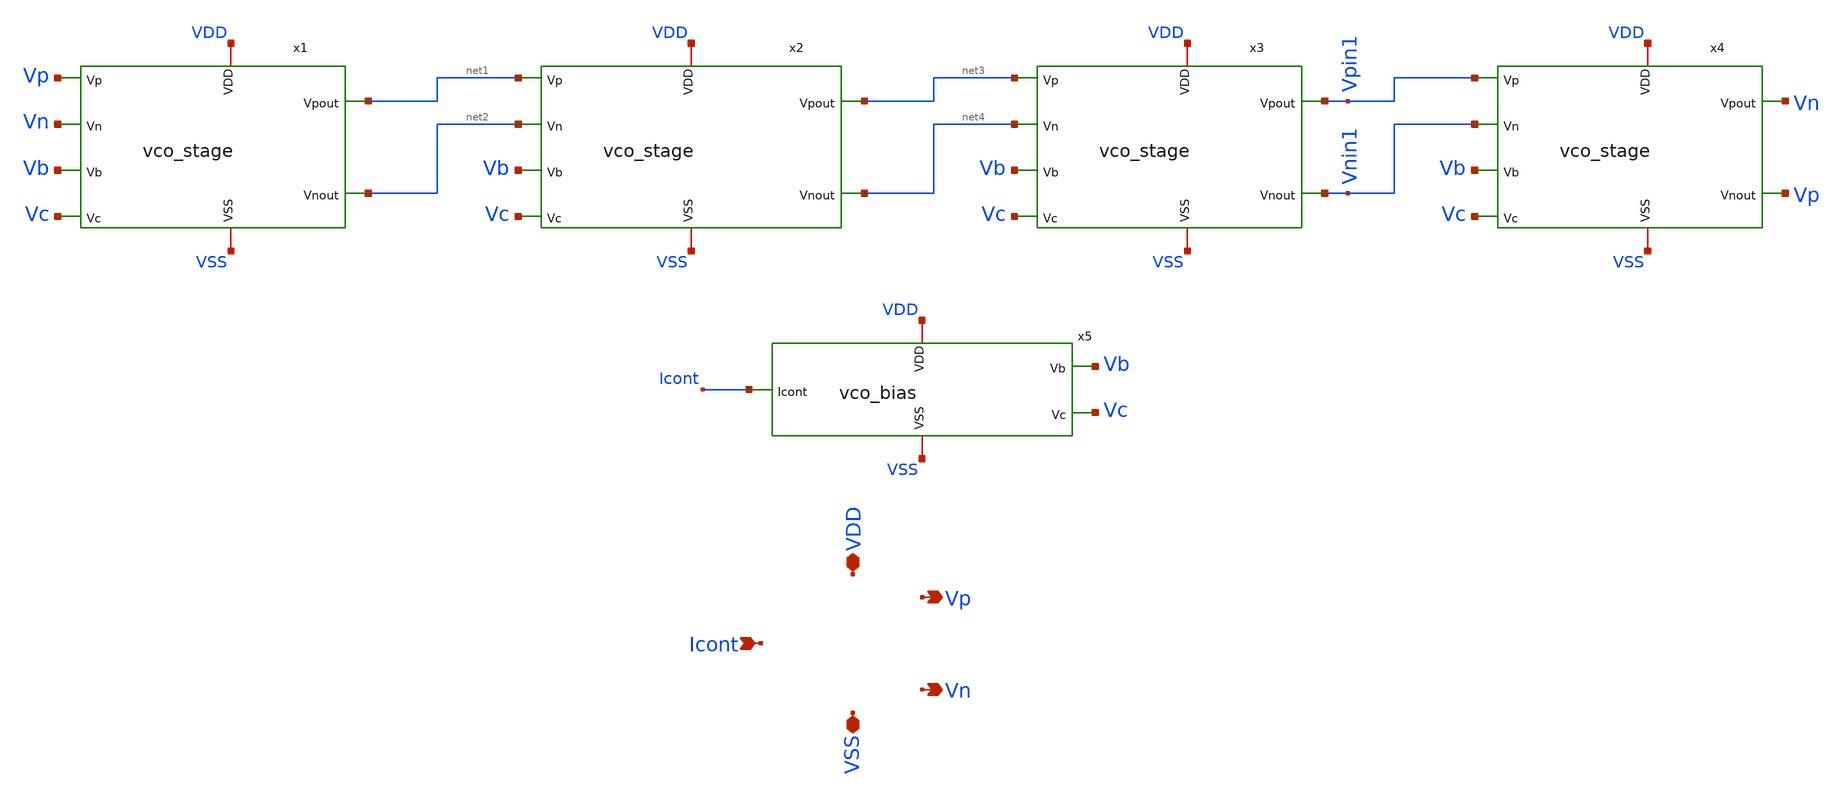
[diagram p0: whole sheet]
** sch_path: xschem/vco.sch
**.subckt vco VDD VSS Icont Vp Vn
*.iopin VDD
*.iopin VSS
*.ipin Icont
*.opin Vp
*.opin Vn
x1 VDD VSS Vp Vn Vb Vc net1 net2 vco_stage
x2 VDD VSS net1 net2 Vb Vc net3 net4 vco_stage
x3 VDD VSS net3 net4 Vb Vc Vpin1 Vnin1 vco_stage
x4 VDD VSS Vpin1 Vnin1 Vb Vc Vn Vp vco_stage
x5 VDD VSS Icont Vb Vc vco_bias
**.ends

* expanding   symbol:  vco_stage.sym # of pins=8
** sym_path: xschem/vco_stage.sym
** sch_path: xschem/vco_stage.sch
.subckt vco_stage VDD VSS Vp Vn Vb Vc Vpout Vnout
*.iopin VDD
*.iopin VSS
*.ipin Vp
*.ipin Vn
*.ipin Vb
*.ipin Vc
*.opin Vpout
*.opin Vnout
XM5 Vds_m5 Vc VSS VSS sky130_fd_pr__nfet_01v8 L={L} W={W} nf=2 ad='int((nf+1)/2) * W/nf * 0.29' as='int((nf+2)/2) * W/nf * 0.29'
+ pd='2*int((nf+1)/2) * (W/nf + 0.29)' ps='2*int((nf+2)/2) * (W/nf + 0.29)' nrd='0.29 / W' nrs='0.29 / W'
+ sa=0 sb=0 sd=0 mult=1 m=1
x1 VDD VSS Vp Vb Vnout Vpout Vds_m5 vco_stage_half
x2 VDD VSS Vn Vb Vpout Vnout Vds_m5 vco_stage_half
.ends


* expanding   symbol:  vco_bias.sym # of pins=5
** sym_path: xschem/vco_bias.sym
** sch_path: xschem/vco_bias.sch
.subckt vco_bias VDD VSS Icont Vb Vc
*.iopin VDD
*.iopin VSS
*.ipin Icont
*.opin Vb
*.opin Vc
XM1 Icont Icont VSS VSS sky130_fd_pr__nfet_01v8 L=1 W=2 nf=2 ad='int((nf+1)/2) * W/nf * 0.29' as='int((nf+2)/2) * W/nf * 0.29'
+ pd='2*int((nf+1)/2) * (W/nf + 0.29)' ps='2*int((nf+2)/2) * (W/nf + 0.29)' nrd='0.29 / W' nrs='0.29 / W'
+ sa=0 sb=0 sd=0 mult=1 m=1
XM2 Vb Icont VSS VSS sky130_fd_pr__nfet_01v8 L=1 W=2 nf=2 ad='int((nf+1)/2) * W/nf * 0.29' as='int((nf+2)/2) * W/nf * 0.29'
+ pd='2*int((nf+1)/2) * (W/nf + 0.29)' ps='2*int((nf+2)/2) * (W/nf + 0.29)' nrd='0.29 / W' nrs='0.29 / W'
+ sa=0 sb=0 sd=0 mult=1 m=1
XM3 VDD Vb Vb VDD sky130_fd_pr__nfet_01v8 L=1 W=2 nf=2 ad='int((nf+1)/2) * W/nf * 0.29' as='int((nf+2)/2) * W/nf * 0.29'
+ pd='2*int((nf+1)/2) * (W/nf + 0.29)' ps='2*int((nf+2)/2) * (W/nf + 0.29)' nrd='0.29 / W' nrs='0.29 / W'
+ sa=0 sb=0 sd=0 mult=1 m=1
V1 Vc Icont 0
.ends


* expanding   symbol:  vco_stage_half.sym # of pins=7
** sym_path: xschem/vco_stage_half.sym
** sch_path: xschem/vco_stage_half.sch
.subckt vco_stage_half VDD VSS Vin Vb Vd Vout Vs
*.iopin VDD
*.iopin VSS
*.ipin Vin
*.ipin Vb
*.ipin Vd
*.opin Vout
*.opin Vs
XM8 VSS Vout VSS VSS sky130_fd_pr__nfet_01v8 L={WLcap} W={WLcap} nf=1 ad='int((nf+1)/2) * W/nf * 0.29'
+ as='int((nf+2)/2) * W/nf * 0.29' pd='2*int((nf+1)/2) * (W/nf + 0.29)' ps='2*int((nf+2)/2) * (W/nf + 0.29)'
+ nrd='0.29 / W' nrs='0.29 / W' sa=0 sb=0 sd=0 mult=1 m=1
XM7 Vout Vd VDD VDD sky130_fd_pr__pfet_01v8 L={L} W={W} nf=2 ad='int((nf+1)/2) * W/nf * 0.29' as='int((nf+2)/2) * W/nf * 0.29'
+ pd='2*int((nf+1)/2) * (W/nf + 0.29)' ps='2*int((nf+2)/2) * (W/nf + 0.29)' nrd='0.29 / W' nrs='0.29 / W'
+ sa=0 sb=0 sd=0 mult=1 m=1
XM3 Vout Vb VDD VDD sky130_fd_pr__pfet_01v8 L={L} W={W} nf=2 ad='int((nf+1)/2) * W/nf * 0.29' as='int((nf+2)/2) * W/nf * 0.29'
+ pd='2*int((nf+1)/2) * (W/nf + 0.29)' ps='2*int((nf+2)/2) * (W/nf + 0.29)' nrd='0.29 / W' nrs='0.29 / W'
+ sa=0 sb=0 sd=0 mult=1 m=1
XM1 Vout Vin Vs VSS sky130_fd_pr__nfet_01v8 L={L} W={W} nf=2 ad='int((nf+1)/2) * W/nf * 0.29' as='int((nf+2)/2) * W/nf * 0.29'
+ pd='2*int((nf+1)/2) * (W/nf + 0.29)' ps='2*int((nf+2)/2) * (W/nf + 0.29)' nrd='0.29 / W' nrs='0.29 / W'
+ sa=0 sb=0 sd=0 mult=1 m=1
.ends

.end
